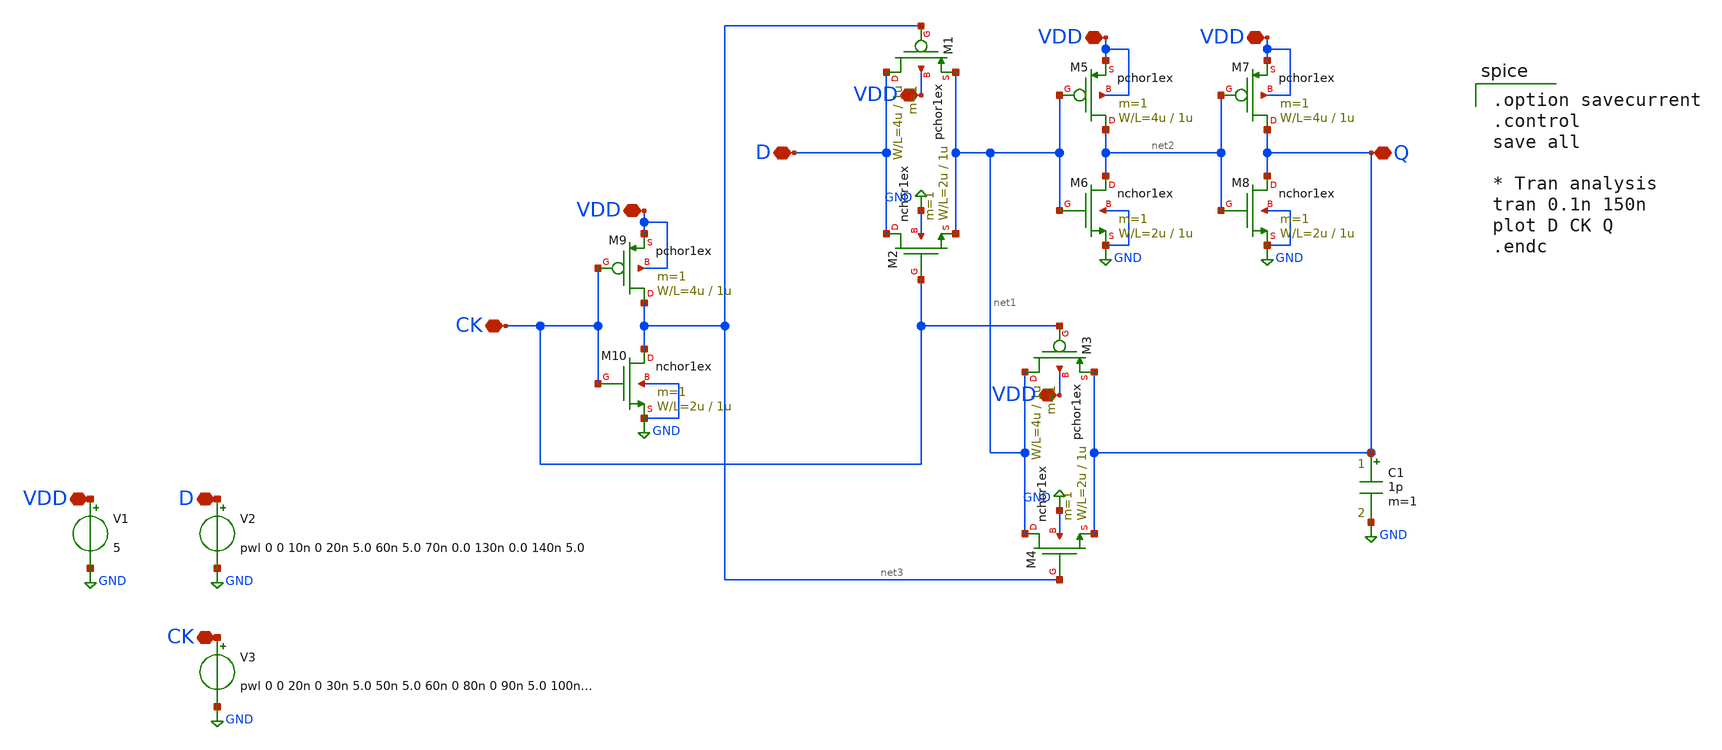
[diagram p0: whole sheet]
** sch_path: member_project/dokunira/Dlatch_layout/Dlatch_sym.sch
**.subckt Dlatch_sym CK D VDD VDD VDD Q VDD D CK VDD VDD
*.iopin CK
*.iopin D
*.iopin VDD
*.iopin VDD
*.iopin VDD
*.iopin Q
*.iopin VDD
*.iopin D
*.iopin CK
*.iopin VDD
*.iopin VDD
M1 D net3 net1 VDD pchor1ex L=1u W=4u m=1
M2 D CK net1 GND nchor1ex L=1u W=2u m=1
M3 net1 CK Q VDD pchor1ex L=1u W=4u m=1
M4 net1 net3 Q GND nchor1ex L=1u W=2u m=1
M5 net2 net1 VDD VDD pchor1ex L=1u W=4u m=1
M6 net2 net1 GND GND nchor1ex L=1u W=2u m=1
M7 Q net2 VDD VDD pchor1ex L=1u W=4u m=1
M8 Q net2 GND GND nchor1ex L=1u W=2u m=1
M9 net3 CK VDD VDD pchor1ex L=1u W=4u m=1
M10 net3 CK GND GND nchor1ex L=1u W=2u m=1
V1 VDD GND 5
V2 D GND pwl 0 0 10n 0 20n 5.0 60n 5.0 70n 0.0 130n 0.0 140n 5.0
V3 CK GND pwl 0 0 20n 0 30n 5.0 50n 5.0 60n 0 80n 0 90n 5.0 100n 5.0 120n 5.0 130n 0.0
C1 Q GND 1p m=1
**** begin user architecture code
 .include $::LIB/mos.lib
.include $::LIB/passive.lib
.include $::LIB/diode.lib

.option savecurrent
.control
save all

* Tran analysis
tran 0.1n 150n
plot D CK Q
.endc


**** end user architecture code
**.ends
.GLOBAL GND
.end
